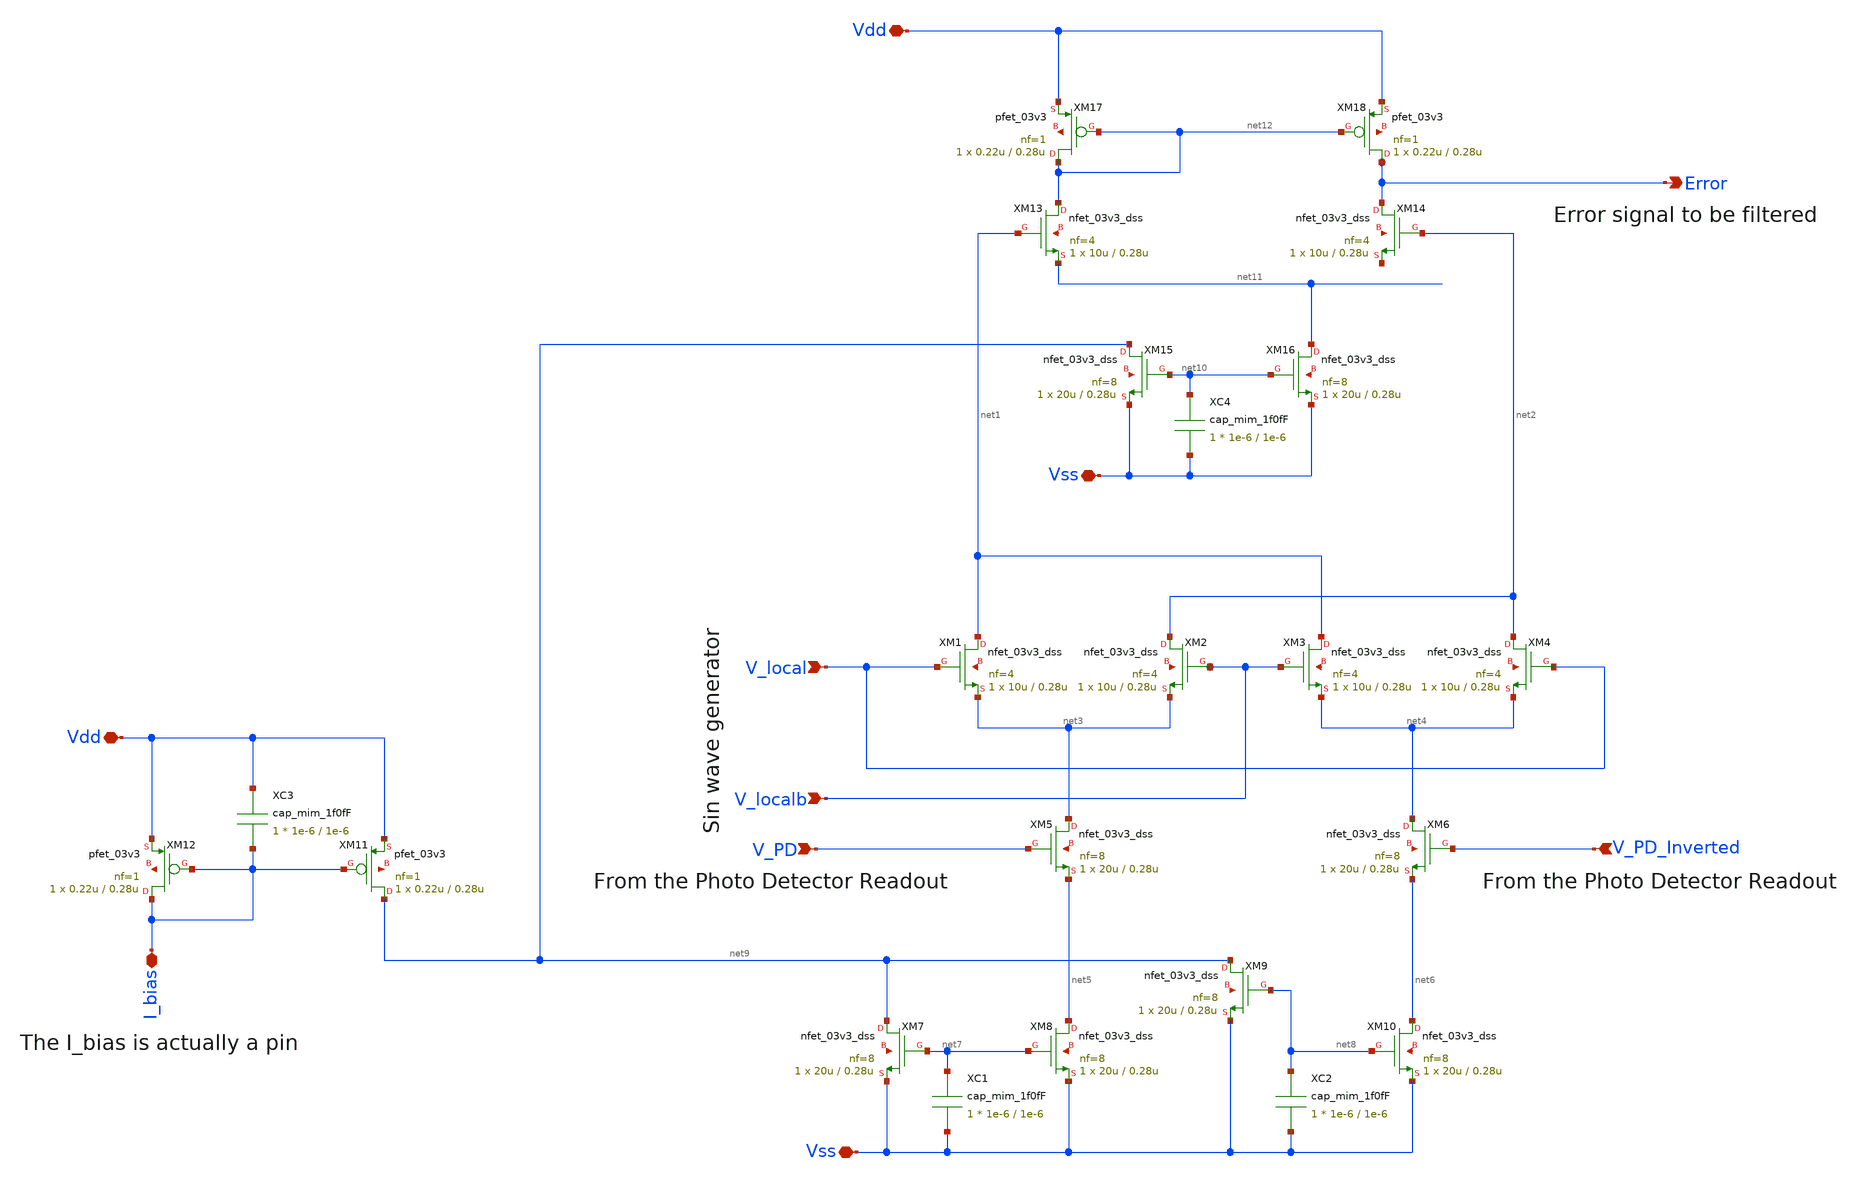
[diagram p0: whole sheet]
** sch_path: Analog/schematics/Legacy/Mixer.sch
**.subckt Mixer V_local Vss V_PD V_localb V_PD_Inverted I_bias Vdd Vss Vdd Error
*.ipin V_local
*.iopin Vss
*.ipin V_PD
*.ipin V_localb
*.ipin V_PD_Inverted
*.iopin I_bias
*.iopin Vdd
*.iopin Vss
*.iopin Vdd
*.opin Error
XM1 net1 V_local net3 net13 nfet_03v3_dss L=0.28u W=10u nf=4 ad='int((nf+1)/2) * W/nf * 0.18u' as='int((nf+2)/2) * W/nf * 0.18u'
+ pd='2*int((nf+1)/2) * (W/nf + 0.18u)' ps='2*int((nf+2)/2) * (W/nf + 0.18u)' nrd='0.18u / W' nrs='0.18u / W'
+ sa=0 sb=0 sd=0 m=1
XM2 net2 V_localb net3 net14 nfet_03v3_dss L=0.28u W=10u nf=4 ad='int((nf+1)/2) * W/nf * 0.18u' as='int((nf+2)/2) * W/nf * 0.18u'
+ pd='2*int((nf+1)/2) * (W/nf + 0.18u)' ps='2*int((nf+2)/2) * (W/nf + 0.18u)' nrd='0.18u / W' nrs='0.18u / W'
+ sa=0 sb=0 sd=0 m=1
XM3 net1 V_localb net4 net15 nfet_03v3_dss L=0.28u W=10u nf=4 ad='int((nf+1)/2) * W/nf * 0.18u' as='int((nf+2)/2) * W/nf * 0.18u'
+ pd='2*int((nf+1)/2) * (W/nf + 0.18u)' ps='2*int((nf+2)/2) * (W/nf + 0.18u)' nrd='0.18u / W' nrs='0.18u / W'
+ sa=0 sb=0 sd=0 m=1
XM4 net2 V_local net4 net16 nfet_03v3_dss L=0.28u W=10u nf=4 ad='int((nf+1)/2) * W/nf * 0.18u' as='int((nf+2)/2) * W/nf * 0.18u'
+ pd='2*int((nf+1)/2) * (W/nf + 0.18u)' ps='2*int((nf+2)/2) * (W/nf + 0.18u)' nrd='0.18u / W' nrs='0.18u / W'
+ sa=0 sb=0 sd=0 m=1
XM5 net3 V_PD net5 net17 nfet_03v3_dss L=0.28u W=20u nf=8 ad='int((nf+1)/2) * W/nf * 0.18u' as='int((nf+2)/2) * W/nf * 0.18u'
+ pd='2*int((nf+1)/2) * (W/nf + 0.18u)' ps='2*int((nf+2)/2) * (W/nf + 0.18u)' nrd='0.18u / W' nrs='0.18u / W'
+ sa=0 sb=0 sd=0 m=1
XM6 net4 V_PD_Inverted net6 net18 nfet_03v3_dss L=0.28u W=20u nf=8 ad='int((nf+1)/2) * W/nf * 0.18u'
+ as='int((nf+2)/2) * W/nf * 0.18u' pd='2*int((nf+1)/2) * (W/nf + 0.18u)' ps='2*int((nf+2)/2) * (W/nf + 0.18u)'
+ nrd='0.18u / W' nrs='0.18u / W' sa=0 sb=0 sd=0 m=1
XM7 net9 net7 Vss net19 nfet_03v3_dss L=0.28u W=20u nf=8 ad='int((nf+1)/2) * W/nf * 0.18u' as='int((nf+2)/2) * W/nf * 0.18u'
+ pd='2*int((nf+1)/2) * (W/nf + 0.18u)' ps='2*int((nf+2)/2) * (W/nf + 0.18u)' nrd='0.18u / W' nrs='0.18u / W'
+ sa=0 sb=0 sd=0 m=1
XM8 net5 net7 Vss net20 nfet_03v3_dss L=0.28u W=20u nf=8 ad='int((nf+1)/2) * W/nf * 0.18u' as='int((nf+2)/2) * W/nf * 0.18u'
+ pd='2*int((nf+1)/2) * (W/nf + 0.18u)' ps='2*int((nf+2)/2) * (W/nf + 0.18u)' nrd='0.18u / W' nrs='0.18u / W'
+ sa=0 sb=0 sd=0 m=1
XC1 net7 Vss cap_mim_1f0fF c_width=1e-6 c_length=1e-6 m=1
XM9 net9 net8 Vss net21 nfet_03v3_dss L=0.28u W=20u nf=8 ad='int((nf+1)/2) * W/nf * 0.18u' as='int((nf+2)/2) * W/nf * 0.18u'
+ pd='2*int((nf+1)/2) * (W/nf + 0.18u)' ps='2*int((nf+2)/2) * (W/nf + 0.18u)' nrd='0.18u / W' nrs='0.18u / W'
+ sa=0 sb=0 sd=0 m=1
XM10 net6 net8 Vss net22 nfet_03v3_dss L=0.28u W=20u nf=8 ad='int((nf+1)/2) * W/nf * 0.18u' as='int((nf+2)/2) * W/nf * 0.18u'
+ pd='2*int((nf+1)/2) * (W/nf + 0.18u)' ps='2*int((nf+2)/2) * (W/nf + 0.18u)' nrd='0.18u / W' nrs='0.18u / W'
+ sa=0 sb=0 sd=0 m=1
XC2 net8 Vss cap_mim_1f0fF c_width=1e-6 c_length=1e-6 m=1
XM11 net9 I_bias Vdd net23 pfet_03v3 L=0.28u W=0.22u nf=1 ad='int((nf+1)/2) * W/nf * 0.18u' as='int((nf+2)/2) * W/nf * 0.18u'
+ pd='2*int((nf+1)/2) * (W/nf + 0.18u)' ps='2*int((nf+2)/2) * (W/nf + 0.18u)' nrd='0.18u / W' nrs='0.18u / W'
+ sa=0 sb=0 sd=0 m=1
XM12 I_bias I_bias Vdd net24 pfet_03v3 L=0.28u W=0.22u nf=1 ad='int((nf+1)/2) * W/nf * 0.18u' as='int((nf+2)/2) * W/nf * 0.18u'
+ pd='2*int((nf+1)/2) * (W/nf + 0.18u)' ps='2*int((nf+2)/2) * (W/nf + 0.18u)' nrd='0.18u / W' nrs='0.18u / W'
+ sa=0 sb=0 sd=0 m=1
XC3 Vdd I_bias cap_mim_1f0fF c_width=1e-6 c_length=1e-6 m=1
XM13 net12 net1 net11 net25 nfet_03v3_dss L=0.28u W=10u nf=4 ad='int((nf+1)/2) * W/nf * 0.18u' as='int((nf+2)/2) * W/nf * 0.18u'
+ pd='2*int((nf+1)/2) * (W/nf + 0.18u)' ps='2*int((nf+2)/2) * (W/nf + 0.18u)' nrd='0.18u / W' nrs='0.18u / W'
+ sa=0 sb=0 sd=0 m=1
XM14 Error net2 net26 net27 nfet_03v3_dss L=0.28u W=10u nf=4 ad='int((nf+1)/2) * W/nf * 0.18u' as='int((nf+2)/2) * W/nf * 0.18u'
+ pd='2*int((nf+1)/2) * (W/nf + 0.18u)' ps='2*int((nf+2)/2) * (W/nf + 0.18u)' nrd='0.18u / W' nrs='0.18u / W'
+ sa=0 sb=0 sd=0 m=1
XM15 net9 net10 Vss net28 nfet_03v3_dss L=0.28u W=20u nf=8 ad='int((nf+1)/2) * W/nf * 0.18u' as='int((nf+2)/2) * W/nf * 0.18u'
+ pd='2*int((nf+1)/2) * (W/nf + 0.18u)' ps='2*int((nf+2)/2) * (W/nf + 0.18u)' nrd='0.18u / W' nrs='0.18u / W'
+ sa=0 sb=0 sd=0 m=1
XM16 net11 net10 Vss net29 nfet_03v3_dss L=0.28u W=20u nf=8 ad='int((nf+1)/2) * W/nf * 0.18u' as='int((nf+2)/2) * W/nf * 0.18u'
+ pd='2*int((nf+1)/2) * (W/nf + 0.18u)' ps='2*int((nf+2)/2) * (W/nf + 0.18u)' nrd='0.18u / W' nrs='0.18u / W'
+ sa=0 sb=0 sd=0 m=1
XC4 net10 Vss cap_mim_1f0fF c_width=1e-6 c_length=1e-6 m=1
XM17 net12 net12 Vdd net30 pfet_03v3 L=0.28u W=0.22u nf=1 ad='int((nf+1)/2) * W/nf * 0.18u' as='int((nf+2)/2) * W/nf * 0.18u'
+ pd='2*int((nf+1)/2) * (W/nf + 0.18u)' ps='2*int((nf+2)/2) * (W/nf + 0.18u)' nrd='0.18u / W' nrs='0.18u / W'
+ sa=0 sb=0 sd=0 m=1
XM18 Error net12 Vdd net31 pfet_03v3 L=0.28u W=0.22u nf=1 ad='int((nf+1)/2) * W/nf * 0.18u' as='int((nf+2)/2) * W/nf * 0.18u'
+ pd='2*int((nf+1)/2) * (W/nf + 0.18u)' ps='2*int((nf+2)/2) * (W/nf + 0.18u)' nrd='0.18u / W' nrs='0.18u / W'
+ sa=0 sb=0 sd=0 m=1
**.ends
.end
